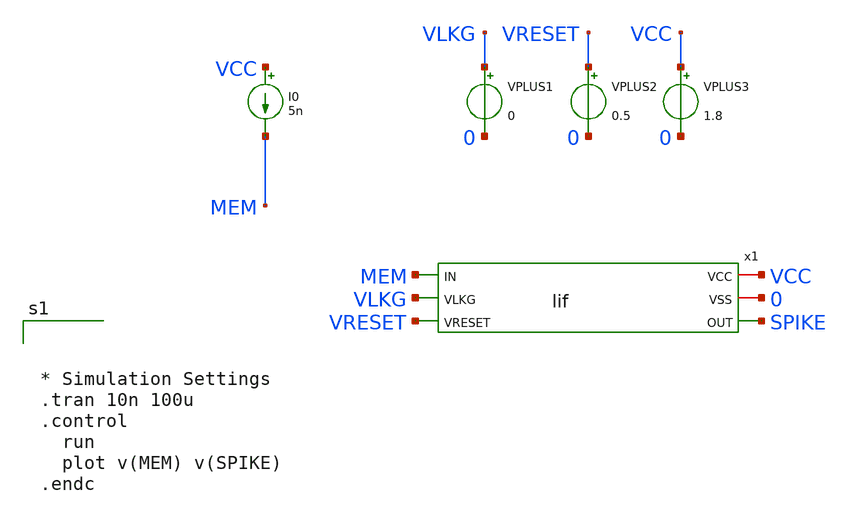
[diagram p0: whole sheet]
** sch_path: xschem/integration.sch
**.subckt integration
VPLUS1 VLKG 0 0
VPLUS2 VRESET 0 0.5
VPLUS3 VCC 0 1.8
I0 VCC MEM 5n
x1 VCC 0 MEM SPIKE VLKG VRESET lif
**** begin user architecture code



* Simulation Settings
.tran 10n 100u
.control
  run
  plot v(MEM) v(SPIKE)
.endc


 .lib $::SKYWATER_MODELS/sky130.lib.spice tt

.include $::SKYWATER_STDCELLS/sky130_fd_sc_hd.spice



**** end user architecture code
**.ends

* expanding   symbol:  lif.sym # of pins=6
** sym_path: xschem/lif.sym
** sch_path: xschem/lif.sch
.subckt lif VCC VSS IN OUT VLKG VRESET
*.iopin VCC
*.iopin VSS
*.ipin IN
*.opin OUT
*.ipin VLKG
*.ipin VRESET
XM1 IN VLKG VSS VSS sky130_fd_pr__nfet_01v8 L=0.15 W=1 nf=1 ad='int((nf+1)/2) * W/nf * 0.29' as='int((nf+2)/2) * W/nf * 0.29'
+ pd='2*int((nf+1)/2) * (W/nf + 0.29)' ps='2*int((nf+2)/2) * (W/nf + 0.29)' nrd='0.29 / W' nrs='0.29 / W'
+ sa=0 sb=0 sd=0 mult=1 m=1
XM2 IN OUT VRESET VSS sky130_fd_pr__nfet_01v8 L=0.15 W=1 nf=1 ad='int((nf+1)/2) * W/nf * 0.29' as='int((nf+2)/2) * W/nf * 0.29'
+ pd='2*int((nf+1)/2) * (W/nf + 0.29)' ps='2*int((nf+2)/2) * (W/nf + 0.29)' nrd='0.29 / W' nrs='0.29 / W'
+ sa=0 sb=0 sd=0 mult=1 m=1
XC1 IN VSS sky130_fd_pr__cap_mim_m3_1 W=1 L=1 MF=12 m=12
x1 VCC VSS OUT IN schmitt_trigger
.ends


* expanding   symbol:  /home/ahmadjabar/tugasakhir/xschem/schmitt_trigger.sym # of pins=4
** sym_path: xschem/schmitt_trigger.sym
** sch_path: xschem/schmitt_trigger.sch
.subckt schmitt_trigger VCC VSS OUT IN
*.ipin IN
*.opin OUT
*.iopin VCC
*.iopin VSS
XM1 net2 IN VCC VCC sky130_fd_pr__pfet_01v8 L=0.15 W=1 nf=1 ad='int((nf+1)/2) * W/nf * 0.29' as='int((nf+2)/2) * W/nf * 0.29'
+ pd='2*int((nf+1)/2) * (W/nf + 0.29)' ps='2*int((nf+2)/2) * (W/nf + 0.29)' nrd='0.29 / W' nrs='0.29 / W'
+ sa=0 sb=0 sd=0 mult=1 m=1
XM2 net3 IN net2 VCC sky130_fd_pr__pfet_01v8 L=0.15 W=1 nf=1 ad='int((nf+1)/2) * W/nf * 0.29' as='int((nf+2)/2) * W/nf * 0.29'
+ pd='2*int((nf+1)/2) * (W/nf + 0.29)' ps='2*int((nf+2)/2) * (W/nf + 0.29)' nrd='0.29 / W' nrs='0.29 / W'
+ sa=0 sb=0 sd=0 mult=1 m=1
XM3 net3 IN net1 VSS sky130_fd_pr__nfet_01v8 L=0.15 W=1 nf=1 ad='int((nf+1)/2) * W/nf * 0.29' as='int((nf+2)/2) * W/nf * 0.29'
+ pd='2*int((nf+1)/2) * (W/nf + 0.29)' ps='2*int((nf+2)/2) * (W/nf + 0.29)' nrd='0.29 / W' nrs='0.29 / W'
+ sa=0 sb=0 sd=0 mult=1 m=1
XM4 net1 IN VSS VSS sky130_fd_pr__nfet_01v8 L=0.15 W=1 nf=1 ad='int((nf+1)/2) * W/nf * 0.29' as='int((nf+2)/2) * W/nf * 0.29'
+ pd='2*int((nf+1)/2) * (W/nf + 0.29)' ps='2*int((nf+2)/2) * (W/nf + 0.29)' nrd='0.29 / W' nrs='0.29 / W'
+ sa=0 sb=0 sd=0 mult=1 m=1
XM5 VSS net3 net2 VCC sky130_fd_pr__pfet_01v8 L=0.15 W=1 nf=1 ad='int((nf+1)/2) * W/nf * 0.29' as='int((nf+2)/2) * W/nf * 0.29'
+ pd='2*int((nf+1)/2) * (W/nf + 0.29)' ps='2*int((nf+2)/2) * (W/nf + 0.29)' nrd='0.29 / W' nrs='0.29 / W'
+ sa=0 sb=0 sd=0 mult=1 m=1
XM6 VCC net3 net1 VSS sky130_fd_pr__nfet_01v8 L=0.15 W=1 nf=1 ad='int((nf+1)/2) * W/nf * 0.29' as='int((nf+2)/2) * W/nf * 0.29'
+ pd='2*int((nf+1)/2) * (W/nf + 0.29)' ps='2*int((nf+2)/2) * (W/nf + 0.29)' nrd='0.29 / W' nrs='0.29 / W'
+ sa=0 sb=0 sd=0 mult=1 m=1
XM7 OUT net3 VSS VSS sky130_fd_pr__nfet_01v8 L=0.15 W=1 nf=1 ad='int((nf+1)/2) * W/nf * 0.29' as='int((nf+2)/2) * W/nf * 0.29'
+ pd='2*int((nf+1)/2) * (W/nf + 0.29)' ps='2*int((nf+2)/2) * (W/nf + 0.29)' nrd='0.29 / W' nrs='0.29 / W'
+ sa=0 sb=0 sd=0 mult=1 m=1
XM8 OUT net3 VCC VCC sky130_fd_pr__pfet_01v8 L=0.15 W=1 nf=1 ad='int((nf+1)/2) * W/nf * 0.29' as='int((nf+2)/2) * W/nf * 0.29'
+ pd='2*int((nf+1)/2) * (W/nf + 0.29)' ps='2*int((nf+2)/2) * (W/nf + 0.29)' nrd='0.29 / W' nrs='0.29 / W'
+ sa=0 sb=0 sd=0 mult=1 m=1
.ends

.end
